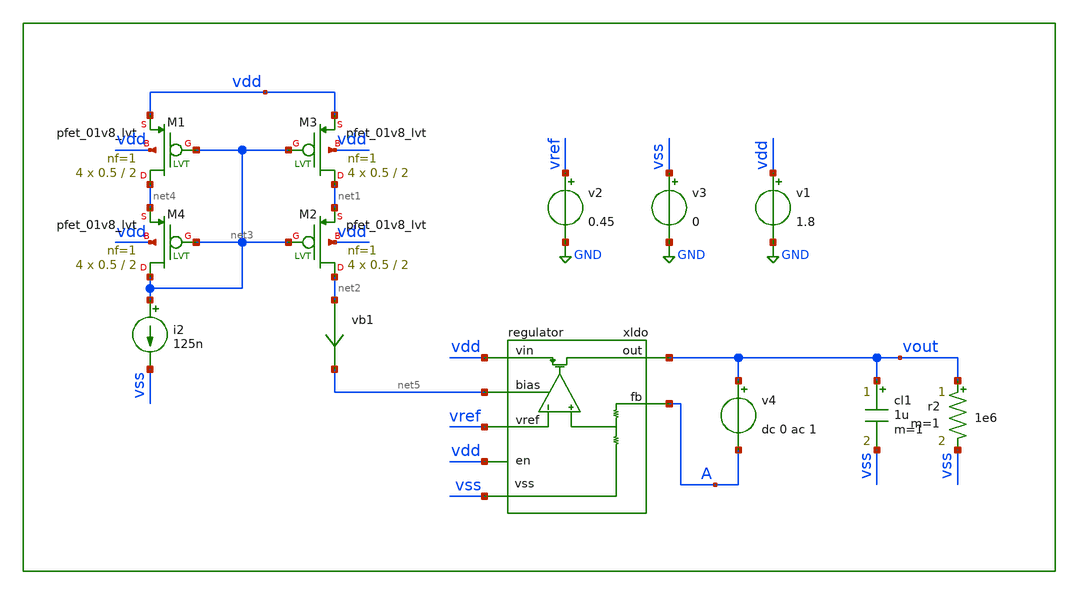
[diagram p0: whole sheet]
** sch_path: xschem/tb/regulator/ac_regulator.sch
**.subckt ac_regulator
v2 vref GND 0.45
xldo vout vref vss vdd net5 vdd A regulator
cl1 vout vss 1u m=1
v4 vout A dc 0 ac 1
r2 vout vss 1e6 m=1
vb1 net2 net5 0
.save i(vb1)
XM2 net2 net3 net1 vdd sky130_fd_pr__pfet_01v8_lvt L=2 W=0.5 nf=1 ad='int((nf+1)/2) * W/nf * 0.29' as='int((nf+2)/2) * W/nf * 0.29'
+ pd='2*int((nf+1)/2) * (W/nf + 0.29)' ps='2*int((nf+2)/2) * (W/nf + 0.29)' nrd='0.29 / W' nrs='0.29 / W'
+ sa=0 sb=0 sd=0 mult=4 m=4
XM4 net3 net3 net4 vdd sky130_fd_pr__pfet_01v8_lvt L=2 W=0.5 nf=1 ad='int((nf+1)/2) * W/nf * 0.29' as='int((nf+2)/2) * W/nf * 0.29'
+ pd='2*int((nf+1)/2) * (W/nf + 0.29)' ps='2*int((nf+2)/2) * (W/nf + 0.29)' nrd='0.29 / W' nrs='0.29 / W'
+ sa=0 sb=0 sd=0 mult=4 m=4
i2 net3 vss 125n
v1 vdd GND 1.8
v3 vss GND 0
XM1 net4 net3 vdd vdd sky130_fd_pr__pfet_01v8_lvt L=2 W=0.5 nf=1 ad='int((nf+1)/2) * W/nf * 0.29' as='int((nf+2)/2) * W/nf * 0.29'
+ pd='2*int((nf+1)/2) * (W/nf + 0.29)' ps='2*int((nf+2)/2) * (W/nf + 0.29)' nrd='0.29 / W' nrs='0.29 / W'
+ sa=0 sb=0 sd=0 mult=4 m=4
XM3 net1 net3 vdd vdd sky130_fd_pr__pfet_01v8_lvt L=2 W=0.5 nf=1 ad='int((nf+1)/2) * W/nf * 0.29' as='int((nf+2)/2) * W/nf * 0.29'
+ pd='2*int((nf+1)/2) * (W/nf + 0.29)' ps='2*int((nf+2)/2) * (W/nf + 0.29)' nrd='0.29 / W' nrs='0.29 / W'
+ sa=0 sb=0 sd=0 mult=4 m=4
**** begin user architecture code

.control
.param MC_SWITCH=0

save all
op
echo ---------------
print vb1#branch
print vout
echo ---------------

ac dec 10 1 100e6
let olg=vout/a
let phase=180/3.14*cph(vout/a)
plot vdb(olg)
plot phase
meas ac ugbw when vdb(olg)=0
meas ac pm find phase when vdb(olg)=0
.endc



* FET CORNERS
.include $::SKYWATER_MODELS/corners/tt.spice
*.include $::SKYWATER_MODELS/corners/ff.spice
*.include $::SKYWATER_MODELS/corners/ss.spice
*.include $::SKYWATER_MODELS/corners/sf.spice
*.include $::SKYWATER_MODELS/corners/fs.spice

* TT + R + C
*.include $::SKYWATER_MODELS/corners/tt_rmax_cmax.spice
*.include $::SKYWATER_MODELS/corners/tt_rmin_cmin.spice
*.include $::SKYWATER_MODELS/corners/tt_rmax_cmin.spice
*.include $::SKYWATER_MODELS/corners/tt_rmin_cmax.spice

* FF + R + C
*.include $::SKYWATER_MODELS/corners/ff_rmax_cmax.spice
*.include $::SKYWATER_MODELS/corners/ff_rmin_cmin.spice
*.include $::SKYWATER_MODELS/corners/ff_rmax_cmin.spice
*.include $::SKYWATER_MODELS/corners/ff_rmin_cmax.spice


* SS + R + C
*.include $::SKYWATER_MODELS/corners/ss_rmax_cmax.spice
*.include $::SKYWATER_MODELS/corners/ss_rmin_cmin.spice
*.include $::SKYWATER_MODELS/corners/ss_rmax_cmin.spice
*.include $::SKYWATER_MODELS/corners/ss_rmin_cmax.spice

* SF + R + C
*.include $::SKYWATER_MODELS/corners/sf_rmax_cmax.spice
*.include $::SKYWATER_MODELS/corners/sf_rmin_cmin.spice
*.include $::SKYWATER_MODELS/corners/sf_rmax_cmin.spice
*.include $::SKYWATER_MODELS/corners/sf_rmin_cmax.spice

* FS + R + C
*.include $::SKYWATER_MODELS/corners/fs_rmax_cmax.spice
*.include $::SKYWATER_MODELS/corners/fs_rmin_cmin.spice
*.include $::SKYWATER_MODELS/corners/fs_rmax_cmin.spice
*.include $::SKYWATER_MODELS/corners/fs_rmin_cmax.spice

**** end user architecture code
**.ends

* expanding   symbol:  regulator/regulator.sym # of pins=7
** sym_path: xschem/regulator/regulator.sym
** sch_path: xschem/regulator/regulator.sch
.subckt regulator out vref vss vin bias en fb
*.iopin vin
*.iopin vss
*.ipin vref
*.opin out
*.iopin bias
*.ipin en
*.ipin fb
XM2 comp vref diff vss sky130_fd_pr__nfet_01v8_lvt L=1 W=1 nf=1 ad='int((nf+1)/2) * W/nf * 0.29' as='int((nf+2)/2) * W/nf * 0.29'
+ pd='2*int((nf+1)/2) * (W/nf + 0.29)' ps='2*int((nf+2)/2) * (W/nf + 0.29)' nrd='0.29 / W' nrs='0.29 / W'
+ sa=0 sb=0 sd=0 mult=8 m=8
XM1 mirr fbdiv diff vss sky130_fd_pr__nfet_01v8_lvt L=1 W=1 nf=1 ad='int((nf+1)/2) * W/nf * 0.29' as='int((nf+2)/2) * W/nf * 0.29'
+ pd='2*int((nf+1)/2) * (W/nf + 0.29)' ps='2*int((nf+2)/2) * (W/nf + 0.29)' nrd='0.29 / W' nrs='0.29 / W'
+ sa=0 sb=0 sd=0 mult=8 m=8
XM5 diff bias vss vss sky130_fd_pr__nfet_01v8_lvt L=1 W=1 nf=1 ad='int((nf+1)/2) * W/nf * 0.29' as='int((nf+2)/2) * W/nf * 0.29'
+ pd='2*int((nf+1)/2) * (W/nf + 0.29)' ps='2*int((nf+2)/2) * (W/nf + 0.29)' nrd='0.29 / W' nrs='0.29 / W'
+ sa=0 sb=0 sd=0 mult=4 m=4
XM4 comp mirr vin vin sky130_fd_pr__pfet_01v8_lvt L=1 W=1 nf=1 ad='int((nf+1)/2) * W/nf * 0.29' as='int((nf+2)/2) * W/nf * 0.29'
+ pd='2*int((nf+1)/2) * (W/nf + 0.29)' ps='2*int((nf+2)/2) * (W/nf + 0.29)' nrd='0.29 / W' nrs='0.29 / W'
+ sa=0 sb=0 sd=0 mult=4 m=4
XM3 mirr mirr vin vin sky130_fd_pr__pfet_01v8_lvt L=1 W=1 nf=1 ad='int((nf+1)/2) * W/nf * 0.29' as='int((nf+2)/2) * W/nf * 0.29'
+ pd='2*int((nf+1)/2) * (W/nf + 0.29)' ps='2*int((nf+2)/2) * (W/nf + 0.29)' nrd='0.29 / W' nrs='0.29 / W'
+ sa=0 sb=0 sd=0 mult=4 m=4
XM6 bias bias vss vss sky130_fd_pr__nfet_01v8_lvt L=1 W=1 nf=1 ad='int((nf+1)/2) * W/nf * 0.29' as='int((nf+2)/2) * W/nf * 0.29'
+ pd='2*int((nf+1)/2) * (W/nf + 0.29)' ps='2*int((nf+2)/2) * (W/nf + 0.29)' nrd='0.29 / W' nrs='0.29 / W'
+ sa=0 sb=0 sd=0 mult=4 m=4
XM7[31] out comp vin vin sky130_fd_pr__pfet_01v8_lvt L=0.5 W=8 nf=1 ad='int((nf+1)/2) * W/nf * 0.29'
+ as='int((nf+2)/2) * W/nf * 0.29' pd='2*int((nf+1)/2) * (W/nf + 0.29)' ps='2*int((nf+2)/2) * (W/nf + 0.29)'
+ nrd='0.29 / W' nrs='0.29 / W' sa=0 sb=0 sd=0 mult=1 m=1
XM7[30] out comp vin vin sky130_fd_pr__pfet_01v8_lvt L=0.5 W=8 nf=1 ad='int((nf+1)/2) * W/nf * 0.29'
+ as='int((nf+2)/2) * W/nf * 0.29' pd='2*int((nf+1)/2) * (W/nf + 0.29)' ps='2*int((nf+2)/2) * (W/nf + 0.29)'
+ nrd='0.29 / W' nrs='0.29 / W' sa=0 sb=0 sd=0 mult=1 m=1
XM7[29] out comp vin vin sky130_fd_pr__pfet_01v8_lvt L=0.5 W=8 nf=1 ad='int((nf+1)/2) * W/nf * 0.29'
+ as='int((nf+2)/2) * W/nf * 0.29' pd='2*int((nf+1)/2) * (W/nf + 0.29)' ps='2*int((nf+2)/2) * (W/nf + 0.29)'
+ nrd='0.29 / W' nrs='0.29 / W' sa=0 sb=0 sd=0 mult=1 m=1
XM7[28] out comp vin vin sky130_fd_pr__pfet_01v8_lvt L=0.5 W=8 nf=1 ad='int((nf+1)/2) * W/nf * 0.29'
+ as='int((nf+2)/2) * W/nf * 0.29' pd='2*int((nf+1)/2) * (W/nf + 0.29)' ps='2*int((nf+2)/2) * (W/nf + 0.29)'
+ nrd='0.29 / W' nrs='0.29 / W' sa=0 sb=0 sd=0 mult=1 m=1
XM7[27] out comp vin vin sky130_fd_pr__pfet_01v8_lvt L=0.5 W=8 nf=1 ad='int((nf+1)/2) * W/nf * 0.29'
+ as='int((nf+2)/2) * W/nf * 0.29' pd='2*int((nf+1)/2) * (W/nf + 0.29)' ps='2*int((nf+2)/2) * (W/nf + 0.29)'
+ nrd='0.29 / W' nrs='0.29 / W' sa=0 sb=0 sd=0 mult=1 m=1
XM7[26] out comp vin vin sky130_fd_pr__pfet_01v8_lvt L=0.5 W=8 nf=1 ad='int((nf+1)/2) * W/nf * 0.29'
+ as='int((nf+2)/2) * W/nf * 0.29' pd='2*int((nf+1)/2) * (W/nf + 0.29)' ps='2*int((nf+2)/2) * (W/nf + 0.29)'
+ nrd='0.29 / W' nrs='0.29 / W' sa=0 sb=0 sd=0 mult=1 m=1
XM7[25] out comp vin vin sky130_fd_pr__pfet_01v8_lvt L=0.5 W=8 nf=1 ad='int((nf+1)/2) * W/nf * 0.29'
+ as='int((nf+2)/2) * W/nf * 0.29' pd='2*int((nf+1)/2) * (W/nf + 0.29)' ps='2*int((nf+2)/2) * (W/nf + 0.29)'
+ nrd='0.29 / W' nrs='0.29 / W' sa=0 sb=0 sd=0 mult=1 m=1
XM7[24] out comp vin vin sky130_fd_pr__pfet_01v8_lvt L=0.5 W=8 nf=1 ad='int((nf+1)/2) * W/nf * 0.29'
+ as='int((nf+2)/2) * W/nf * 0.29' pd='2*int((nf+1)/2) * (W/nf + 0.29)' ps='2*int((nf+2)/2) * (W/nf + 0.29)'
+ nrd='0.29 / W' nrs='0.29 / W' sa=0 sb=0 sd=0 mult=1 m=1
XM7[23] out comp vin vin sky130_fd_pr__pfet_01v8_lvt L=0.5 W=8 nf=1 ad='int((nf+1)/2) * W/nf * 0.29'
+ as='int((nf+2)/2) * W/nf * 0.29' pd='2*int((nf+1)/2) * (W/nf + 0.29)' ps='2*int((nf+2)/2) * (W/nf + 0.29)'
+ nrd='0.29 / W' nrs='0.29 / W' sa=0 sb=0 sd=0 mult=1 m=1
XM7[22] out comp vin vin sky130_fd_pr__pfet_01v8_lvt L=0.5 W=8 nf=1 ad='int((nf+1)/2) * W/nf * 0.29'
+ as='int((nf+2)/2) * W/nf * 0.29' pd='2*int((nf+1)/2) * (W/nf + 0.29)' ps='2*int((nf+2)/2) * (W/nf + 0.29)'
+ nrd='0.29 / W' nrs='0.29 / W' sa=0 sb=0 sd=0 mult=1 m=1
XM7[21] out comp vin vin sky130_fd_pr__pfet_01v8_lvt L=0.5 W=8 nf=1 ad='int((nf+1)/2) * W/nf * 0.29'
+ as='int((nf+2)/2) * W/nf * 0.29' pd='2*int((nf+1)/2) * (W/nf + 0.29)' ps='2*int((nf+2)/2) * (W/nf + 0.29)'
+ nrd='0.29 / W' nrs='0.29 / W' sa=0 sb=0 sd=0 mult=1 m=1
XM7[20] out comp vin vin sky130_fd_pr__pfet_01v8_lvt L=0.5 W=8 nf=1 ad='int((nf+1)/2) * W/nf * 0.29'
+ as='int((nf+2)/2) * W/nf * 0.29' pd='2*int((nf+1)/2) * (W/nf + 0.29)' ps='2*int((nf+2)/2) * (W/nf + 0.29)'
+ nrd='0.29 / W' nrs='0.29 / W' sa=0 sb=0 sd=0 mult=1 m=1
XM7[19] out comp vin vin sky130_fd_pr__pfet_01v8_lvt L=0.5 W=8 nf=1 ad='int((nf+1)/2) * W/nf * 0.29'
+ as='int((nf+2)/2) * W/nf * 0.29' pd='2*int((nf+1)/2) * (W/nf + 0.29)' ps='2*int((nf+2)/2) * (W/nf + 0.29)'
+ nrd='0.29 / W' nrs='0.29 / W' sa=0 sb=0 sd=0 mult=1 m=1
XM7[18] out comp vin vin sky130_fd_pr__pfet_01v8_lvt L=0.5 W=8 nf=1 ad='int((nf+1)/2) * W/nf * 0.29'
+ as='int((nf+2)/2) * W/nf * 0.29' pd='2*int((nf+1)/2) * (W/nf + 0.29)' ps='2*int((nf+2)/2) * (W/nf + 0.29)'
+ nrd='0.29 / W' nrs='0.29 / W' sa=0 sb=0 sd=0 mult=1 m=1
XM7[17] out comp vin vin sky130_fd_pr__pfet_01v8_lvt L=0.5 W=8 nf=1 ad='int((nf+1)/2) * W/nf * 0.29'
+ as='int((nf+2)/2) * W/nf * 0.29' pd='2*int((nf+1)/2) * (W/nf + 0.29)' ps='2*int((nf+2)/2) * (W/nf + 0.29)'
+ nrd='0.29 / W' nrs='0.29 / W' sa=0 sb=0 sd=0 mult=1 m=1
XM7[16] out comp vin vin sky130_fd_pr__pfet_01v8_lvt L=0.5 W=8 nf=1 ad='int((nf+1)/2) * W/nf * 0.29'
+ as='int((nf+2)/2) * W/nf * 0.29' pd='2*int((nf+1)/2) * (W/nf + 0.29)' ps='2*int((nf+2)/2) * (W/nf + 0.29)'
+ nrd='0.29 / W' nrs='0.29 / W' sa=0 sb=0 sd=0 mult=1 m=1
XM7[15] out comp vin vin sky130_fd_pr__pfet_01v8_lvt L=0.5 W=8 nf=1 ad='int((nf+1)/2) * W/nf * 0.29'
+ as='int((nf+2)/2) * W/nf * 0.29' pd='2*int((nf+1)/2) * (W/nf + 0.29)' ps='2*int((nf+2)/2) * (W/nf + 0.29)'
+ nrd='0.29 / W' nrs='0.29 / W' sa=0 sb=0 sd=0 mult=1 m=1
XM7[14] out comp vin vin sky130_fd_pr__pfet_01v8_lvt L=0.5 W=8 nf=1 ad='int((nf+1)/2) * W/nf * 0.29'
+ as='int((nf+2)/2) * W/nf * 0.29' pd='2*int((nf+1)/2) * (W/nf + 0.29)' ps='2*int((nf+2)/2) * (W/nf + 0.29)'
+ nrd='0.29 / W' nrs='0.29 / W' sa=0 sb=0 sd=0 mult=1 m=1
XM7[13] out comp vin vin sky130_fd_pr__pfet_01v8_lvt L=0.5 W=8 nf=1 ad='int((nf+1)/2) * W/nf * 0.29'
+ as='int((nf+2)/2) * W/nf * 0.29' pd='2*int((nf+1)/2) * (W/nf + 0.29)' ps='2*int((nf+2)/2) * (W/nf + 0.29)'
+ nrd='0.29 / W' nrs='0.29 / W' sa=0 sb=0 sd=0 mult=1 m=1
XM7[12] out comp vin vin sky130_fd_pr__pfet_01v8_lvt L=0.5 W=8 nf=1 ad='int((nf+1)/2) * W/nf * 0.29'
+ as='int((nf+2)/2) * W/nf * 0.29' pd='2*int((nf+1)/2) * (W/nf + 0.29)' ps='2*int((nf+2)/2) * (W/nf + 0.29)'
+ nrd='0.29 / W' nrs='0.29 / W' sa=0 sb=0 sd=0 mult=1 m=1
XM7[11] out comp vin vin sky130_fd_pr__pfet_01v8_lvt L=0.5 W=8 nf=1 ad='int((nf+1)/2) * W/nf * 0.29'
+ as='int((nf+2)/2) * W/nf * 0.29' pd='2*int((nf+1)/2) * (W/nf + 0.29)' ps='2*int((nf+2)/2) * (W/nf + 0.29)'
+ nrd='0.29 / W' nrs='0.29 / W' sa=0 sb=0 sd=0 mult=1 m=1
XM7[10] out comp vin vin sky130_fd_pr__pfet_01v8_lvt L=0.5 W=8 nf=1 ad='int((nf+1)/2) * W/nf * 0.29'
+ as='int((nf+2)/2) * W/nf * 0.29' pd='2*int((nf+1)/2) * (W/nf + 0.29)' ps='2*int((nf+2)/2) * (W/nf + 0.29)'
+ nrd='0.29 / W' nrs='0.29 / W' sa=0 sb=0 sd=0 mult=1 m=1
XM7[9] out comp vin vin sky130_fd_pr__pfet_01v8_lvt L=0.5 W=8 nf=1 ad='int((nf+1)/2) * W/nf * 0.29' as='int((nf+2)/2) * W/nf * 0.29'
+ pd='2*int((nf+1)/2) * (W/nf + 0.29)' ps='2*int((nf+2)/2) * (W/nf + 0.29)' nrd='0.29 / W' nrs='0.29 / W'
+ sa=0 sb=0 sd=0 mult=1 m=1
XM7[8] out comp vin vin sky130_fd_pr__pfet_01v8_lvt L=0.5 W=8 nf=1 ad='int((nf+1)/2) * W/nf * 0.29' as='int((nf+2)/2) * W/nf * 0.29'
+ pd='2*int((nf+1)/2) * (W/nf + 0.29)' ps='2*int((nf+2)/2) * (W/nf + 0.29)' nrd='0.29 / W' nrs='0.29 / W'
+ sa=0 sb=0 sd=0 mult=1 m=1
XM7[7] out comp vin vin sky130_fd_pr__pfet_01v8_lvt L=0.5 W=8 nf=1 ad='int((nf+1)/2) * W/nf * 0.29' as='int((nf+2)/2) * W/nf * 0.29'
+ pd='2*int((nf+1)/2) * (W/nf + 0.29)' ps='2*int((nf+2)/2) * (W/nf + 0.29)' nrd='0.29 / W' nrs='0.29 / W'
+ sa=0 sb=0 sd=0 mult=1 m=1
XM7[6] out comp vin vin sky130_fd_pr__pfet_01v8_lvt L=0.5 W=8 nf=1 ad='int((nf+1)/2) * W/nf * 0.29' as='int((nf+2)/2) * W/nf * 0.29'
+ pd='2*int((nf+1)/2) * (W/nf + 0.29)' ps='2*int((nf+2)/2) * (W/nf + 0.29)' nrd='0.29 / W' nrs='0.29 / W'
+ sa=0 sb=0 sd=0 mult=1 m=1
XM7[5] out comp vin vin sky130_fd_pr__pfet_01v8_lvt L=0.5 W=8 nf=1 ad='int((nf+1)/2) * W/nf * 0.29' as='int((nf+2)/2) * W/nf * 0.29'
+ pd='2*int((nf+1)/2) * (W/nf + 0.29)' ps='2*int((nf+2)/2) * (W/nf + 0.29)' nrd='0.29 / W' nrs='0.29 / W'
+ sa=0 sb=0 sd=0 mult=1 m=1
XM7[4] out comp vin vin sky130_fd_pr__pfet_01v8_lvt L=0.5 W=8 nf=1 ad='int((nf+1)/2) * W/nf * 0.29' as='int((nf+2)/2) * W/nf * 0.29'
+ pd='2*int((nf+1)/2) * (W/nf + 0.29)' ps='2*int((nf+2)/2) * (W/nf + 0.29)' nrd='0.29 / W' nrs='0.29 / W'
+ sa=0 sb=0 sd=0 mult=1 m=1
XM7[3] out comp vin vin sky130_fd_pr__pfet_01v8_lvt L=0.5 W=8 nf=1 ad='int((nf+1)/2) * W/nf * 0.29' as='int((nf+2)/2) * W/nf * 0.29'
+ pd='2*int((nf+1)/2) * (W/nf + 0.29)' ps='2*int((nf+2)/2) * (W/nf + 0.29)' nrd='0.29 / W' nrs='0.29 / W'
+ sa=0 sb=0 sd=0 mult=1 m=1
XM7[2] out comp vin vin sky130_fd_pr__pfet_01v8_lvt L=0.5 W=8 nf=1 ad='int((nf+1)/2) * W/nf * 0.29' as='int((nf+2)/2) * W/nf * 0.29'
+ pd='2*int((nf+1)/2) * (W/nf + 0.29)' ps='2*int((nf+2)/2) * (W/nf + 0.29)' nrd='0.29 / W' nrs='0.29 / W'
+ sa=0 sb=0 sd=0 mult=1 m=1
XM7[1] out comp vin vin sky130_fd_pr__pfet_01v8_lvt L=0.5 W=8 nf=1 ad='int((nf+1)/2) * W/nf * 0.29' as='int((nf+2)/2) * W/nf * 0.29'
+ pd='2*int((nf+1)/2) * (W/nf + 0.29)' ps='2*int((nf+2)/2) * (W/nf + 0.29)' nrd='0.29 / W' nrs='0.29 / W'
+ sa=0 sb=0 sd=0 mult=1 m=1
XM7[0] out comp vin vin sky130_fd_pr__pfet_01v8_lvt L=0.5 W=8 nf=1 ad='int((nf+1)/2) * W/nf * 0.29' as='int((nf+2)/2) * W/nf * 0.29'
+ pd='2*int((nf+1)/2) * (W/nf + 0.29)' ps='2*int((nf+2)/2) * (W/nf + 0.29)' nrd='0.29 / W' nrs='0.29 / W'
+ sa=0 sb=0 sd=0 mult=1 m=1
XC1 out comp sky130_fd_pr__cap_mim_m3_1 W=5 L=5 MF=8 m=8
XM9 bias enb vss vss sky130_fd_pr__nfet_01v8_lvt L=0.4 W=1 nf=1 ad='int((nf+1)/2) * W/nf * 0.29' as='int((nf+2)/2) * W/nf * 0.29'
+ pd='2*int((nf+1)/2) * (W/nf + 0.29)' ps='2*int((nf+2)/2) * (W/nf + 0.29)' nrd='0.29 / W' nrs='0.29 / W'
+ sa=0 sb=0 sd=0 mult=1 m=1
x1 vin en enb vss inv_lvt
XM8 comp en vin vin sky130_fd_pr__pfet_01v8_lvt L=0.4 W=1 nf=1 ad='int((nf+1)/2) * W/nf * 0.29' as='int((nf+2)/2) * W/nf * 0.29'
+ pd='2*int((nf+1)/2) * (W/nf + 0.29)' ps='2*int((nf+2)/2) * (W/nf + 0.29)' nrd='0.29 / W' nrs='0.29 / W'
+ sa=0 sb=0 sd=0 mult=1 m=1
XM10 bias bias bias vss sky130_fd_pr__nfet_01v8_lvt L=1 W=1 nf=1 ad='int((nf+1)/2) * W/nf * 0.29' as='int((nf+2)/2) * W/nf * 0.29'
+ pd='2*int((nf+1)/2) * (W/nf + 0.29)' ps='2*int((nf+2)/2) * (W/nf + 0.29)' nrd='0.29 / W' nrs='0.29 / W'
+ sa=0 sb=0 sd=0 mult=4 m=4
XM11 diff bias diff vss sky130_fd_pr__nfet_01v8_lvt L=1 W=1 nf=1 ad='int((nf+1)/2) * W/nf * 0.29' as='int((nf+2)/2) * W/nf * 0.29'
+ pd='2*int((nf+1)/2) * (W/nf + 0.29)' ps='2*int((nf+2)/2) * (W/nf + 0.29)' nrd='0.29 / W' nrs='0.29 / W'
+ sa=0 sb=0 sd=0 mult=4 m=4
XM12 comp comp comp vss sky130_fd_pr__nfet_01v8_lvt L=1 W=1 nf=1 ad='int((nf+1)/2) * W/nf * 0.29' as='int((nf+2)/2) * W/nf * 0.29'
+ pd='2*int((nf+1)/2) * (W/nf + 0.29)' ps='2*int((nf+2)/2) * (W/nf + 0.29)' nrd='0.29 / W' nrs='0.29 / W'
+ sa=0 sb=0 sd=0 mult=2 m=2
XM13 mirr mirr mirr vss sky130_fd_pr__nfet_01v8_lvt L=1 W=1 nf=1 ad='int((nf+1)/2) * W/nf * 0.29' as='int((nf+2)/2) * W/nf * 0.29'
+ pd='2*int((nf+1)/2) * (W/nf + 0.29)' ps='2*int((nf+2)/2) * (W/nf + 0.29)' nrd='0.29 / W' nrs='0.29 / W'
+ sa=0 sb=0 sd=0 mult=2 m=2
XM15 mirr mirr mirr vin sky130_fd_pr__pfet_01v8_lvt L=1 W=1 nf=1 ad='int((nf+1)/2) * W/nf * 0.29' as='int((nf+2)/2) * W/nf * 0.29'
+ pd='2*int((nf+1)/2) * (W/nf + 0.29)' ps='2*int((nf+2)/2) * (W/nf + 0.29)' nrd='0.29 / W' nrs='0.29 / W'
+ sa=0 sb=0 sd=0 mult=2 m=2
XM16 comp mirr comp vin sky130_fd_pr__pfet_01v8_lvt L=1 W=1 nf=1 ad='int((nf+1)/2) * W/nf * 0.29' as='int((nf+2)/2) * W/nf * 0.29'
+ pd='2*int((nf+1)/2) * (W/nf + 0.29)' ps='2*int((nf+2)/2) * (W/nf + 0.29)' nrd='0.29 / W' nrs='0.29 / W'
+ sa=0 sb=0 sd=0 mult=2 m=2
XR2 fbdiv fb vss sky130_fd_pr__res_xhigh_po L=34 mult=1 m=1
XR1 vss fbdiv vss sky130_fd_pr__res_xhigh_po L=34 mult=1 m=1
XR3[1] vss vss vss sky130_fd_pr__res_xhigh_po L=8.5 mult=1 m=1
XR3[0] vss vss vss sky130_fd_pr__res_xhigh_po L=8.5 mult=1 m=1
.ends


* expanding   symbol:  logic/inv_lvt.sym # of pins=4
** sym_path: xschem/logic/inv_lvt.sym
** sch_path: xschem/logic/inv_lvt.sch
.subckt inv_lvt vdd in out vss
*.iopin vdd
*.iopin vss
*.ipin in
*.opin out
XM1 out in vss vss sky130_fd_pr__nfet_01v8_lvt L=0.4 W=1 nf=1 ad='int((nf+1)/2) * W/nf * 0.29' as='int((nf+2)/2) * W/nf * 0.29'
+ pd='2*int((nf+1)/2) * (W/nf + 0.29)' ps='2*int((nf+2)/2) * (W/nf + 0.29)' nrd='0.29 / W' nrs='0.29 / W'
+ sa=0 sb=0 sd=0 mult=1 m=1
XM2 out in vdd vdd sky130_fd_pr__pfet_01v8_lvt L=0.4 W=1 nf=1 ad='int((nf+1)/2) * W/nf * 0.29' as='int((nf+2)/2) * W/nf * 0.29'
+ pd='2*int((nf+1)/2) * (W/nf + 0.29)' ps='2*int((nf+2)/2) * (W/nf + 0.29)' nrd='0.29 / W' nrs='0.29 / W'
+ sa=0 sb=0 sd=0 mult=1 m=1
.ends

.GLOBAL GND
.end
